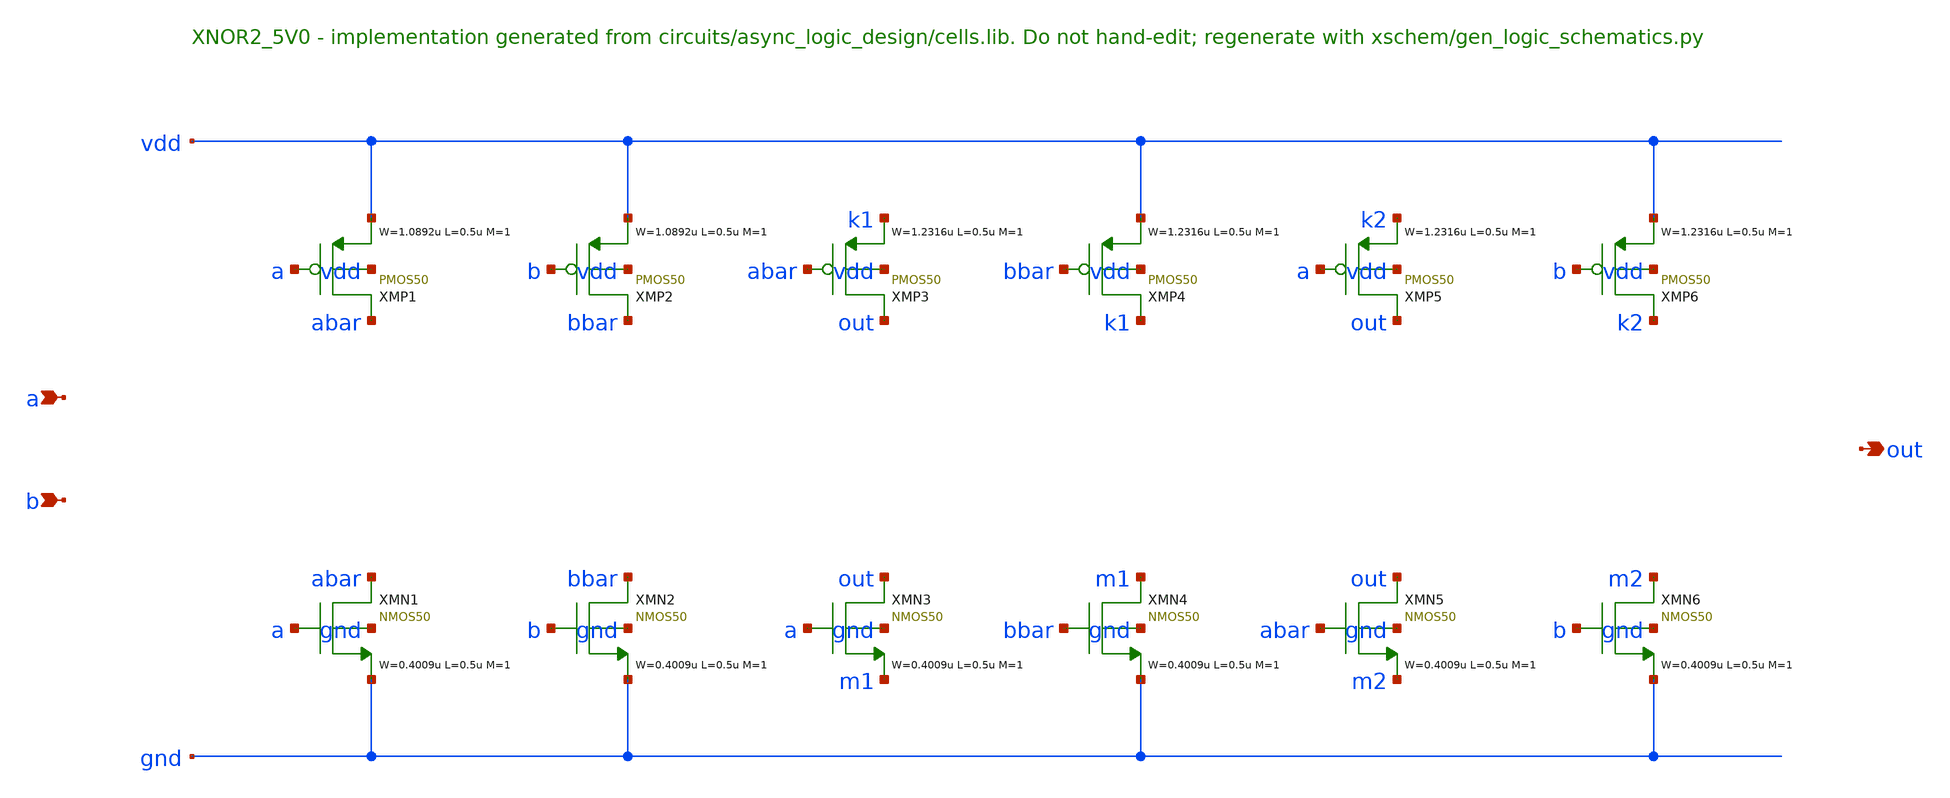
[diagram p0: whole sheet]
** sch_path: xschem/logic/XNOR2_5V0.sch
**.subckt XNOR2_5V0 a b out
*.ipin a
*.ipin b
*.opin out
XMP1 abar a vdd vdd PMOS50 W=1.0892u L=0.5u M=1 MM_SIGMA=0
XMP2 bbar b vdd vdd PMOS50 W=1.0892u L=0.5u M=1 MM_SIGMA=0
XMP3 out abar k1 vdd PMOS50 W=1.2316u L=0.5u M=1 MM_SIGMA=0
XMP4 k1 bbar vdd vdd PMOS50 W=1.2316u L=0.5u M=1 MM_SIGMA=0
XMP5 out a k2 vdd PMOS50 W=1.2316u L=0.5u M=1 MM_SIGMA=0
XMP6 k2 b vdd vdd PMOS50 W=1.2316u L=0.5u M=1 MM_SIGMA=0
XMN1 abar a gnd gnd NMOS50 W=0.4009u L=0.5u M=1 MM_SIGMA=0
XMN2 bbar b gnd gnd NMOS50 W=0.4009u L=0.5u M=1 MM_SIGMA=0
XMN3 out a m1 gnd NMOS50 W=0.4009u L=0.5u M=1 MM_SIGMA=0
XMN4 m1 bbar gnd gnd NMOS50 W=0.4009u L=0.5u M=1 MM_SIGMA=0
XMN5 out abar m2 gnd NMOS50 W=0.4009u L=0.5u M=1 MM_SIGMA=0
XMN6 m2 b gnd gnd NMOS50 W=0.4009u L=0.5u M=1 MM_SIGMA=0
**.ends
.end
